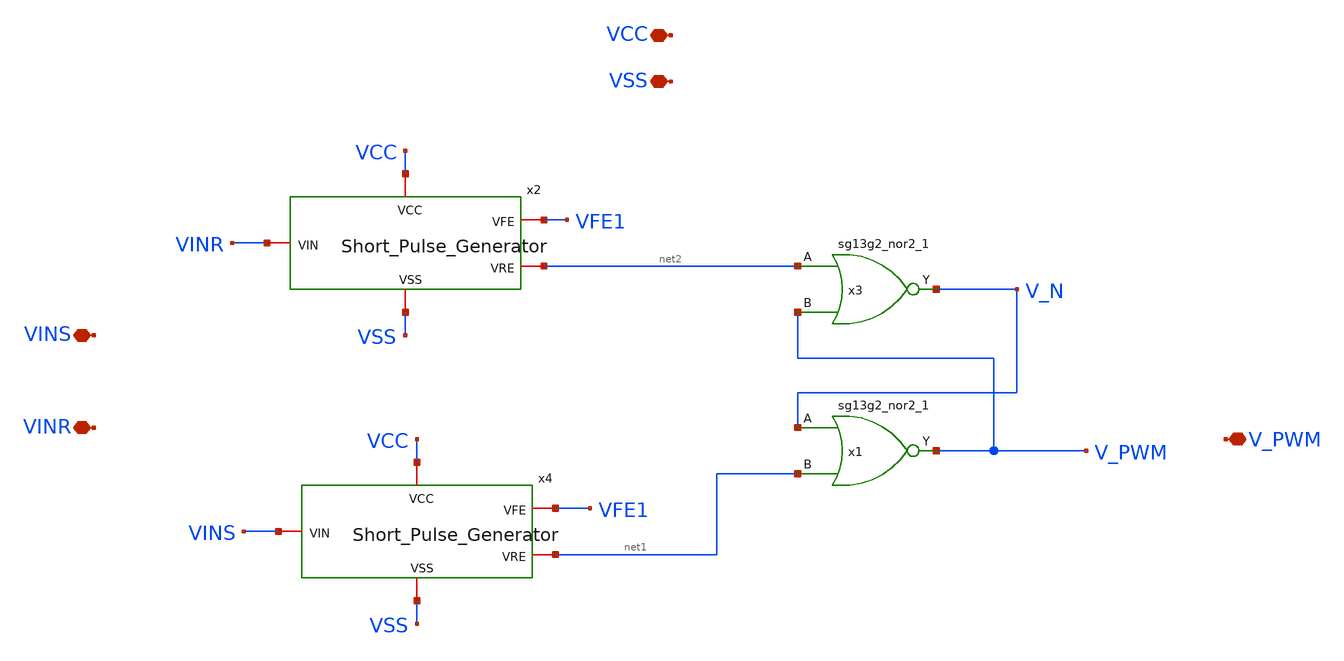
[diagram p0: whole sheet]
** sch_path: xschem/IHP_Tapeout24_AMsent20241028/PhaseDetector.sch
**.subckt PhaseDetector V_PWM VCC VSS VINS VINR
*.iopin V_PWM
*.iopin VCC
*.iopin VSS
*.iopin VINS
*.iopin VINR
x3 V_N net2 V_PWM VCC VSS sg13g2_nor2_1
x1 V_PWM V_N net1 VCC VSS sg13g2_nor2_1
x2 VCC VSS VFE1 VINR net2 Short_Pulse_Generator
x4 VCC VSS VFE1 VINS net1 Short_Pulse_Generator
**.ends
.end
